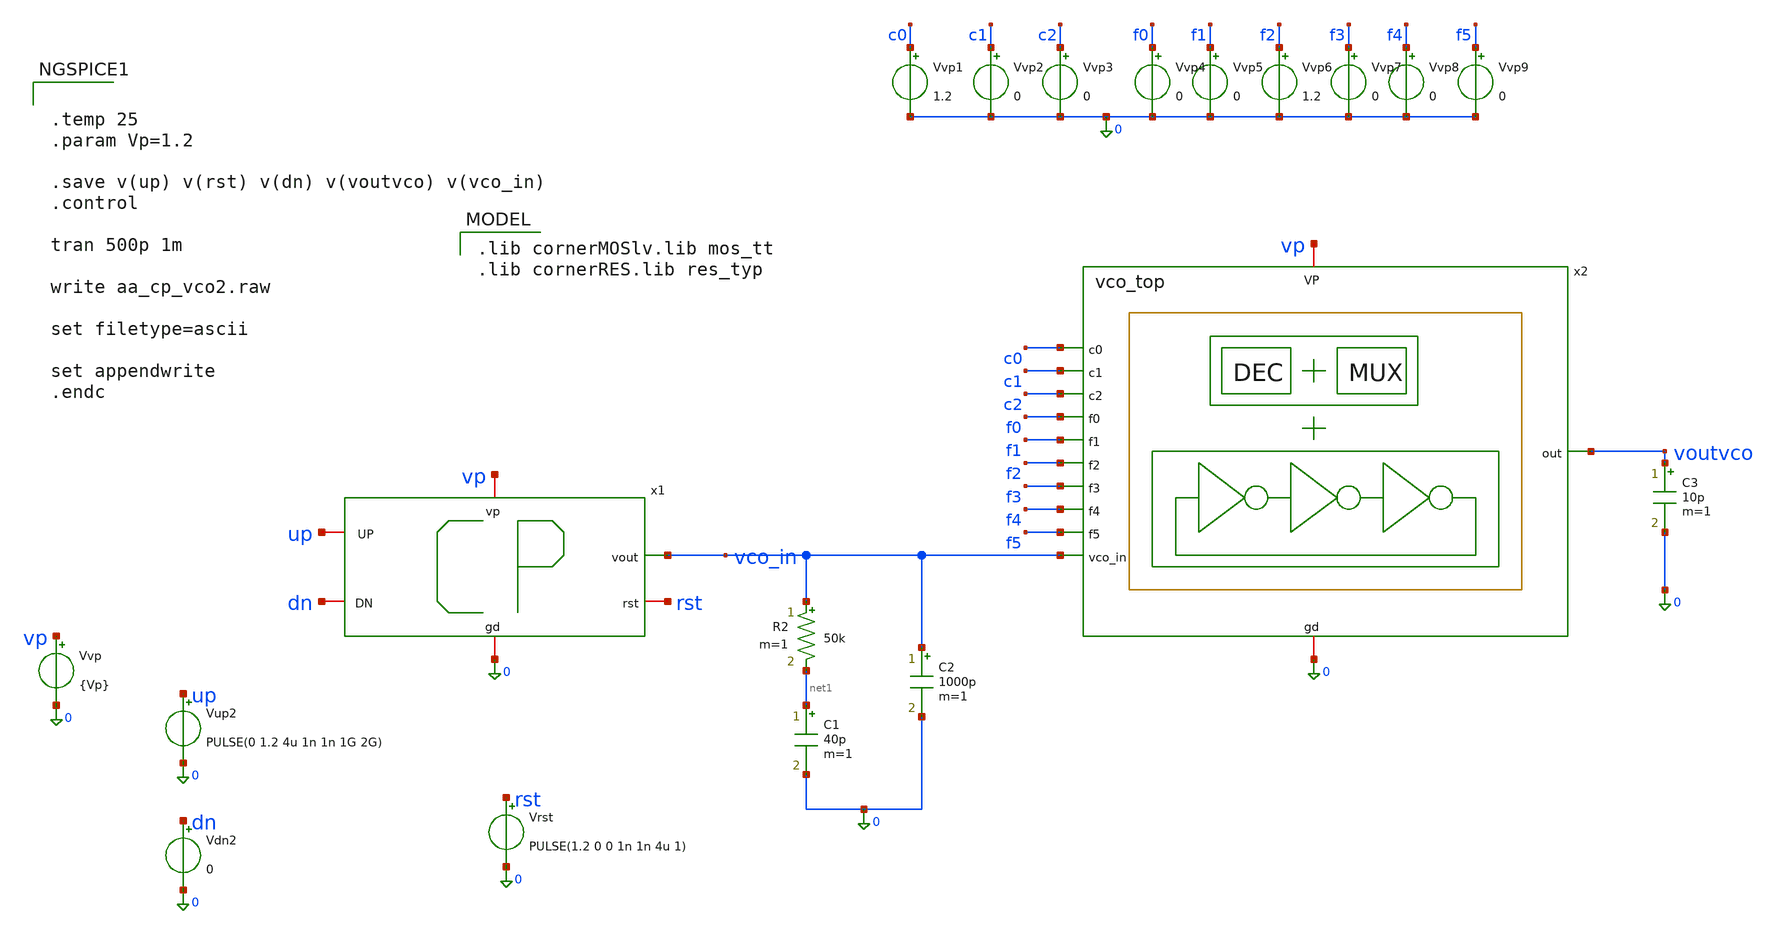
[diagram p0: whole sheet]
** sch_path: schematics/charge_pump/cp10u_fullvco_tb.sch
**.subckt cp10u_fullvco_tb
R2 vco_in net1 50k m=1
C1 net1 0 40p m=1
C2 vco_in 0 1000p m=1
Vvp vp 0 {Vp}
Vup2 up 0 PULSE(0 1.2 4u 1n 1n 1G 2G)
Vdn2 dn 0 0
Vvp1 c0 0 1.2
Vvp2 c1 0 0
Vvp3 c2 0 0
Vvp4 f0 0 0
Vvp5 f1 0 0
Vvp6 f2 0 1.2
Vvp7 f3 0 0
Vvp8 f4 0 0
Vrst rst 0 PULSE(1.2 0 0 1n 1n 4u 1)
Vvp9 f5 0 0
x2 voutvco 0 vp c0 c1 c2 f0 f1 f2 f3 f4 f5 vco_in vco_top
C3 voutvco 0 10p m=1
x1 vp up vco_in dn rst 0 charge_pump_cell
**** begin user architecture code
 .lib cornerMOSlv.lib mos_tt
.lib cornerRES.lib res_typ






.temp 25
.param Vp=1.2

.save v(up) v(rst) v(dn) v(voutvco) v(vco_in)
.control

tran 500p 1m

write aa_cp_vco2.raw

set filetype=ascii

set appendwrite
.endc


**** end user architecture code
**.ends
.end
